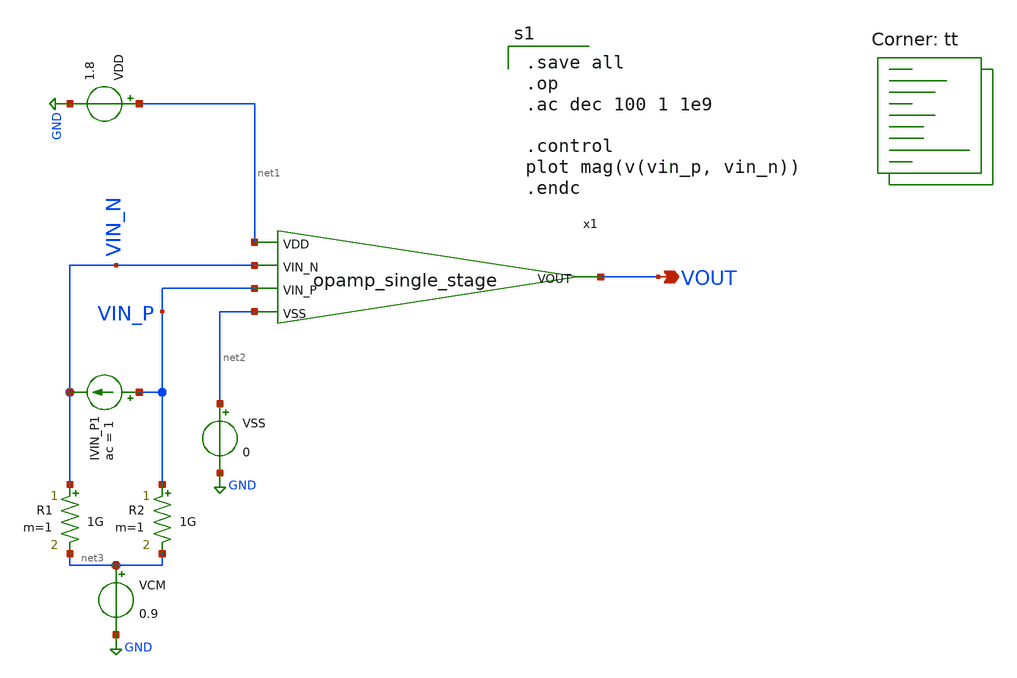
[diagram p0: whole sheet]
** sch_path: analog/schematics/testbenches/tb_impedance.sch
**.subckt tb_impedance VOUT
*.opin VOUT
VDD net1 GND 1.8
VSS net2 GND 0
x1 net1 VOUT VIN_N VIN_P net2 opamp_single_stage
R1 VIN_N net3 1G m=1
VCM net3 GND 0.9
R2 VIN_P net3 1G m=1
IVIN_P1 VIN_P VIN_N ac = 1
**** begin user architecture code
.lib $::SKYWATER_MODELS/sky130.lib.spice tt

.save all
.op
.ac dec 100 1 1e9

.control
plot mag(v(vin_p, vin_n))
.endc

**** end user architecture code
**.ends

* expanding   symbol:  opamp_single_stage.sym # of pins=5
** sym_path: analog/schematics/opamp_single_stage.sym
** sch_path: analog/schematics/opamp_single_stage.sch
.subckt opamp_single_stage VDD VOUT VIN_N VIN_P VSS
*.ipin VDD
*.ipin VIN_P
*.ipin VIN_N
*.ipin VSS
*.opin VOUT
XM4 net2 net1 VDD VDD sky130_fd_pr__pfet_01v8 L=0.5 W=8 nf=1 ad='int((nf+1)/2) * W/nf * 0.29' as='int((nf+2)/2) * W/nf * 0.29'
+ pd='2*int((nf+1)/2) * (W/nf + 0.29)' ps='2*int((nf+2)/2) * (W/nf + 0.29)' nrd='0.29 / W' nrs='0.29 / W'
+ sa=0 sb=0 sd=0 mult=1 m=1
XM3 net1 net1 VDD VDD sky130_fd_pr__pfet_01v8 L=0.5 W=8 nf=1 ad='int((nf+1)/2) * W/nf * 0.29' as='int((nf+2)/2) * W/nf * 0.29'
+ pd='2*int((nf+1)/2) * (W/nf + 0.29)' ps='2*int((nf+2)/2) * (W/nf + 0.29)' nrd='0.29 / W' nrs='0.29 / W'
+ sa=0 sb=0 sd=0 mult=1 m=1
XM1 net1 VIN_P net3 GND sky130_fd_pr__nfet_01v8_lvt L=0.5 W=6 nf=1 ad='int((nf+1)/2) * W/nf * 0.29' as='int((nf+2)/2) * W/nf * 0.29'
+ pd='2*int((nf+1)/2) * (W/nf + 0.29)' ps='2*int((nf+2)/2) * (W/nf + 0.29)' nrd='0.29 / W' nrs='0.29 / W'
+ sa=0 sb=0 sd=0 mult=1 m=1
XM2 net2 VIN_N net3 GND sky130_fd_pr__nfet_01v8_lvt L=0.5 W=6 nf=1 ad='int((nf+1)/2) * W/nf * 0.29' as='int((nf+2)/2) * W/nf * 0.29'
+ pd='2*int((nf+1)/2) * (W/nf + 0.29)' ps='2*int((nf+2)/2) * (W/nf + 0.29)' nrd='0.29 / W' nrs='0.29 / W'
+ sa=0 sb=0 sd=0 mult=1 m=1
XM5 VOUT net2 VDD VDD sky130_fd_pr__pfet_01v8 L=0.5 W=20 nf=1 ad='int((nf+1)/2) * W/nf * 0.29' as='int((nf+2)/2) * W/nf * 0.29'
+ pd='2*int((nf+1)/2) * (W/nf + 0.29)' ps='2*int((nf+2)/2) * (W/nf + 0.29)' nrd='0.29 / W' nrs='0.29 / W'
+ sa=0 sb=0 sd=0 mult=1 m=1
XC1 net5 VOUT sky130_fd_pr__cap_mim_m3_1 W=25 L=20 MF=1 m=1
XM8 net4 net4 VSS VSS sky130_fd_pr__nfet_01v8_lvt L=1.0 W=2 nf=1 ad='int((nf+1)/2) * W/nf * 0.29' as='int((nf+2)/2) * W/nf * 0.29'
+ pd='2*int((nf+1)/2) * (W/nf + 0.29)' ps='2*int((nf+2)/2) * (W/nf + 0.29)' nrd='0.29 / W' nrs='0.29 / W'
+ sa=0 sb=0 sd=0 mult=1 m=1
XM7 net3 net4 VSS VSS sky130_fd_pr__nfet_01v8_lvt L=1.0 W=4 nf=1 ad='int((nf+1)/2) * W/nf * 0.29' as='int((nf+2)/2) * W/nf * 0.29'
+ pd='2*int((nf+1)/2) * (W/nf + 0.29)' ps='2*int((nf+2)/2) * (W/nf + 0.29)' nrd='0.29 / W' nrs='0.29 / W'
+ sa=0 sb=0 sd=0 mult=1 m=1
XM6 VOUT net4 VSS VSS sky130_fd_pr__nfet_01v8_lvt L=1.0 W=8 nf=1 ad='int((nf+1)/2) * W/nf * 0.29' as='int((nf+2)/2) * W/nf * 0.29'
+ pd='2*int((nf+1)/2) * (W/nf + 0.29)' ps='2*int((nf+2)/2) * (W/nf + 0.29)' nrd='0.29 / W' nrs='0.29 / W'
+ sa=0 sb=0 sd=0 mult=1 m=1
I0 VDD net4 5u
R1 net5 net2 7k m=1
.ends

.GLOBAL GND
.end
